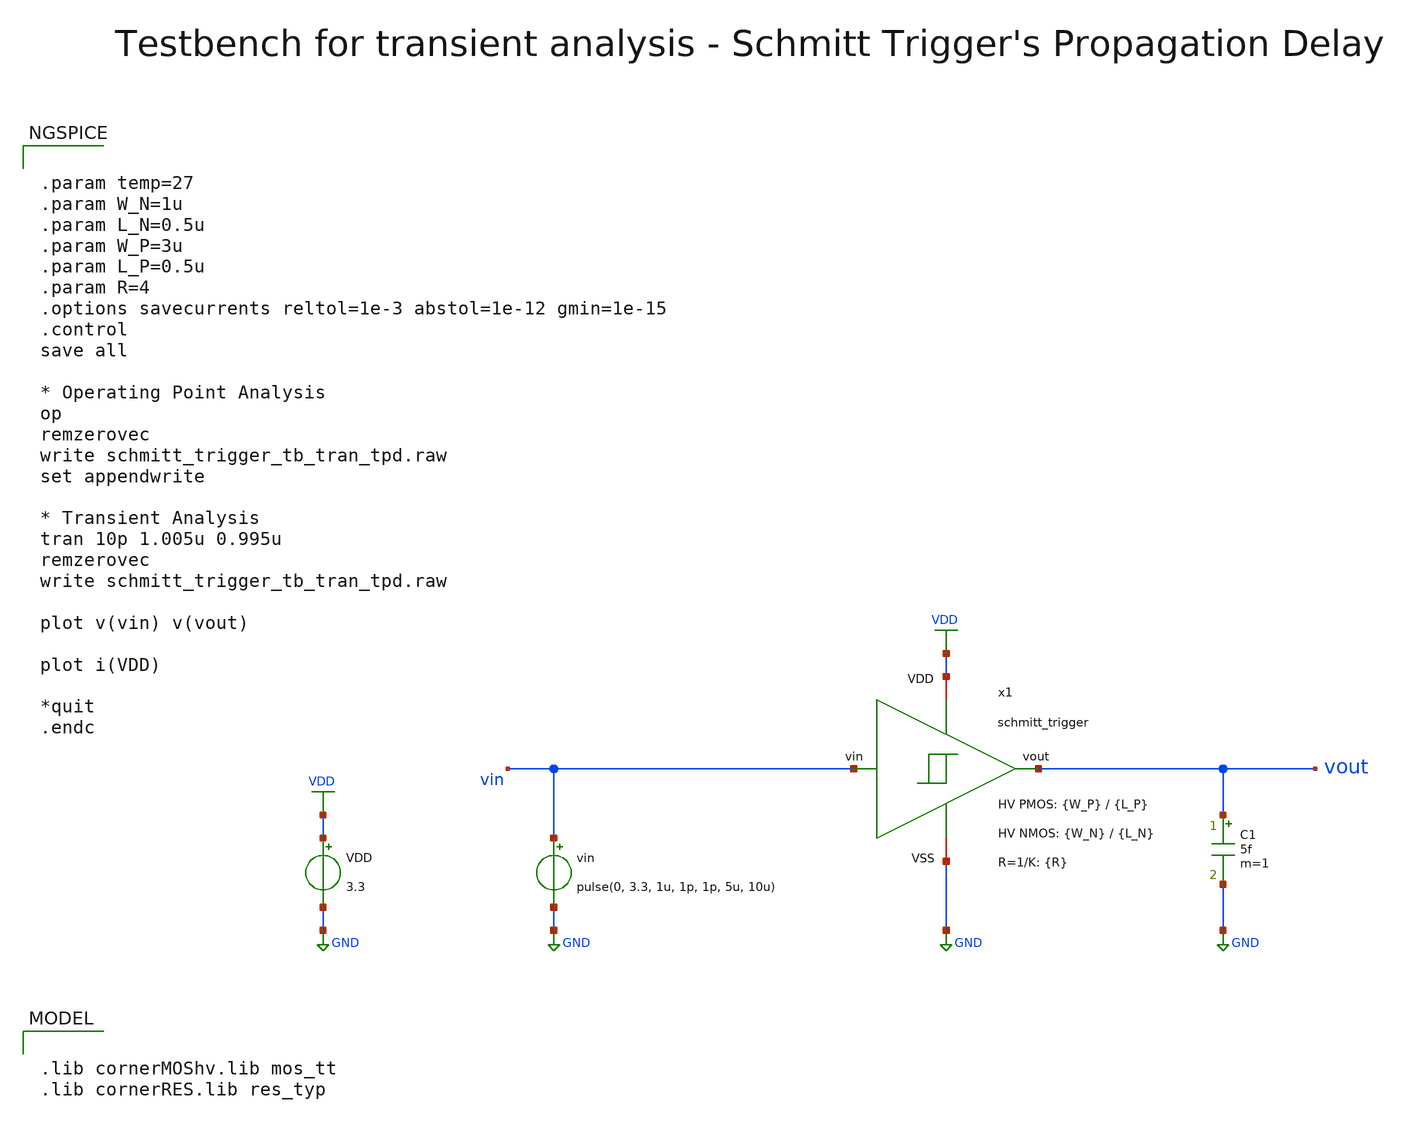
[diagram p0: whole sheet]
** sch_path: SG13G2_ATBS-ADC-main/xschem/schmitt_trigger/testbenches/schmitt_trigger_tb_tran_tpd.sch
**.subckt schmitt_trigger_tb_tran_tpd
C1 vout GND 5f m=1
vin vin GND pulse(0, 3.3, 1u, 1p, 1p, 5u, 10u)
VDD VDD GND 3.3
x1 VDD vout vin GND schmitt_trigger W_P_ST={W_P} L_P_ST={L_P} W_N_ST={W_N} L_N_ST={L_N} R={R}
**** begin user architecture code

.lib cornerMOShv.lib mos_tt
.lib cornerRES.lib res_typ



.param temp=27
.param W_N=1u
.param L_N=0.5u
.param W_P=3u
.param L_P=0.5u
.param R=4
.options savecurrents reltol=1e-3 abstol=1e-12 gmin=1e-15
.control
save all

* Operating Point Analysis
op
remzerovec
write schmitt_trigger_tb_tran_tpd.raw
set appendwrite

* Transient Analysis
tran 10p 1.005u 0.995u
remzerovec
write schmitt_trigger_tb_tran_tpd.raw

plot v(vin) v(vout)

plot i(VDD)

*quit
.endc

**** end user architecture code
**.ends

* expanding   symbol:  schmitt_trigger/schmitt_trigger.sym # of pins=4
** sym_path: SG13G2_ATBS-ADC-main/xschem/schmitt_trigger/schmitt_trigger.sym
** sch_path: SG13G2_ATBS-ADC-main/xschem/schmitt_trigger/schmitt_trigger.sch
.subckt schmitt_trigger VDD vout vin VSS  W_P_ST=3.0u L_P_ST=0.50u W_N_ST=1.0u L_N_ST=0.50u R=4
*.iopin VDD
*.opin vout
*.iopin VSS
*.ipin vin
x1 VDD net2 vout VSS inverter_hv W_P=W_P_ST L_P=L_P_ST W_N=W_N_ST L_N=L_N_ST
XM5 net3 vin VDD VDD sg13_hv_pmos w=W_P_ST l=L_P_ST ng=1 m=1 mm_ok=1
XM4 net2 vin net3 VDD sg13_hv_pmos w=W_P_ST l=L_P_ST ng=1 m=1 mm_ok=1
XM6 VSS net2 net3 VDD sg13_hv_pmos w=R*W_P_ST l=L_P_ST ng=1 m=1 mm_ok=1
XM1 net1 vin VSS VSS sg13_hv_nmos w=W_N_ST l=L_N_ST ng=1 m=1 mm_ok=1
XM2 net2 vin net1 VSS sg13_hv_nmos w=W_N_ST l=L_N_ST ng=1 m=1 mm_ok=1
XM3 VDD net2 net1 VSS sg13_hv_nmos w=R*W_N_ST l=L_N_ST ng=1 m=1 mm_ok=1
.ends


* expanding   symbol:  inverter/inverter_hv.sym # of pins=4
** sym_path: SG13G2_ATBS-ADC-main/xschem/inverter/inverter_hv.sym
** sch_path: SG13G2_ATBS-ADC-main/xschem/inverter/inverter_hv.sch
.subckt inverter_hv VDD vin vout VSS  W_P=3.0u L_P=0.50u W_N=1.0u L_N=0.50u
*.ipin vin
*.iopin VDD
*.iopin VSS
*.opin vout
XM1 vout vin VDD VDD sg13_hv_pmos w=W_P l=L_P ng=1 m=1 mm_ok=1
XM2 vout vin VSS VSS sg13_hv_nmos w=W_N l=L_N ng=1 m=1 mm_ok=1
.ends

.GLOBAL VDD
.GLOBAL GND
.end
